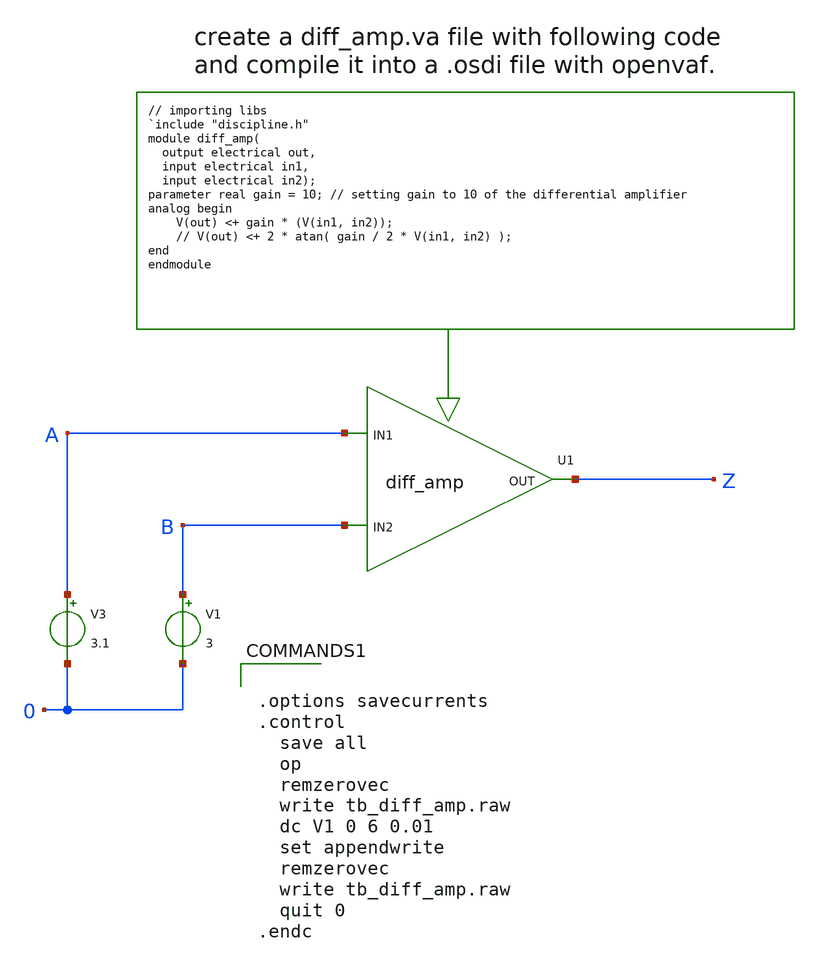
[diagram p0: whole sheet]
** sch_path: schematics/tb_diff_amp.sch
**.subckt tb_diff_amp
V3 A 0 3.1
V1 B 0 3
XU1 Z A B diff_amp_cell
**** begin user architecture code


.options savecurrents
.control
  save all
  op
  remzerovec
  write tb_diff_amp.raw
  dc V1 0 6 0.01
  set appendwrite
  remzerovec
  write tb_diff_amp.raw
  quit 0
.endc


**** end user architecture code
**.ends
**** begin user architecture code

.subckt diff_amp_cell OUT IN1 IN2
N1 out in1 in2 diff_amp_model
.ends diff_amp_cell

.model diff_amp_model diff_amp

.control
* following line specifies the location for the .osdi file so ngspice can use it.
pre_osdi $working_dir/schematics/verilog_a/diff_amp.osdi
.endc

**** end user architecture code
.end
